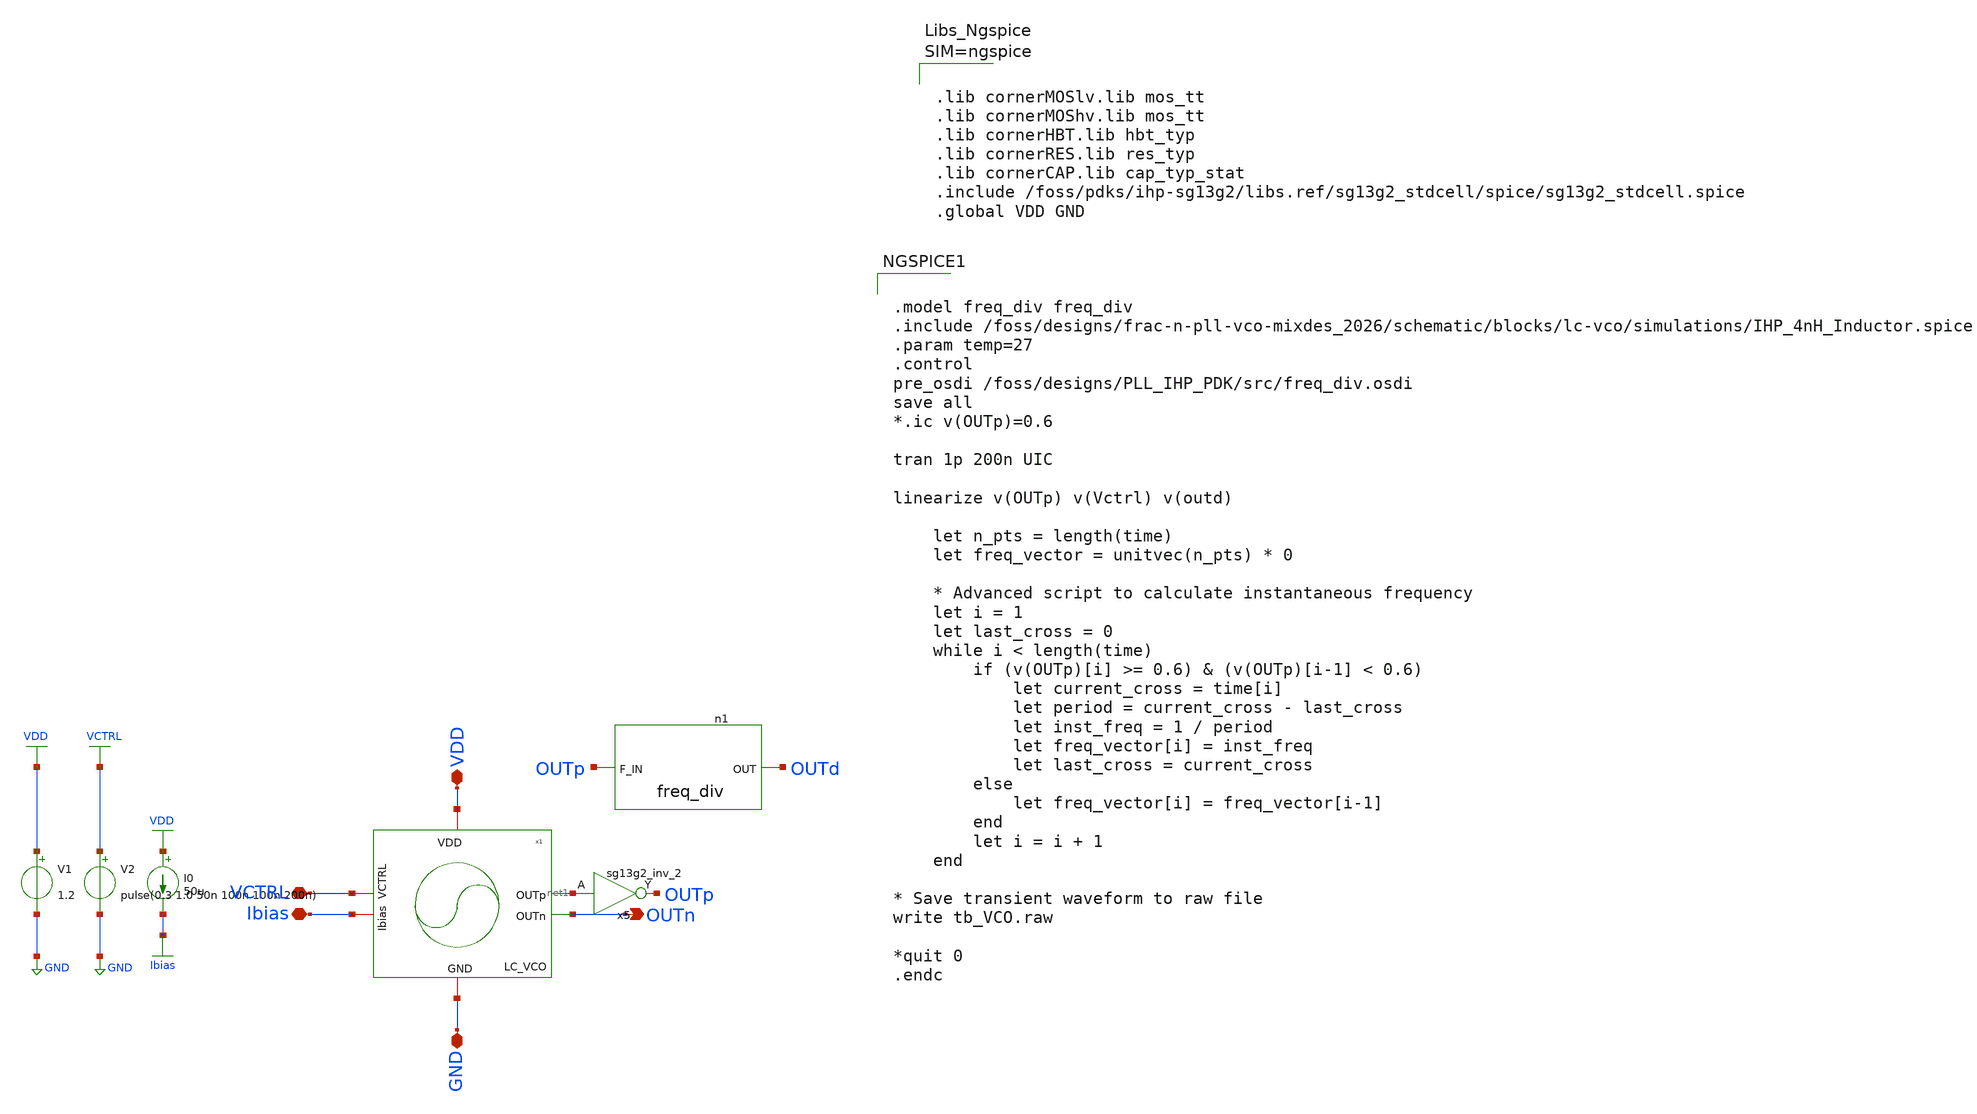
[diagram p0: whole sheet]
** sch_path: schematic/blocks/PLL_IHP/tb/tb_VCO.sch
* IHP-GmbH/IHP-Open-PDK/ihp-sg13g2/libs.tech/xschem/sg13g2_stdcells/sg13g2_inv_2.sch:
* Copyright 2023 IHP PDK Authors
* Licensed under the Apache License, Version 2.0 (the "License");
**.subckt tb_VCO OUTn VDD VCTRL GND Ibias
*.opin OUTn
*.iopin VDD
*.iopin VCTRL
*.iopin GND
*.iopin Ibias
V1 VDD GND 1.2
V2 VCTRL GND pulse(0.3 1.0 50n 100n 100n 200n)
I0 VDD Ibias 50u
x2 VDD net1 OUTn Ibias VCTRL GND LC_VCO
n1 OUTd OUTp freq_div
x5 OUTp net1 VDD GND sg13g2_inv_2
**** begin user architecture code


.model freq_div freq_div
.include /foss/designs/frac-n-pll-vco-mixdes_2026/schematic/blocks/lc-vco/simulations/IHP_4nH_Inductor.spice
.param temp=27
.control
pre_osdi /foss/designs/PLL_IHP_PDK/src/freq_div.osdi
save all
*.ic v(OUTp)=0.6

tran 1p 200n UIC

linearize v(OUTp) v(Vctrl) v(outd)

    let n_pts = length(time)
    let freq_vector = unitvec(n_pts) * 0

    * Advanced script to calculate instantaneous frequency
    let i = 1
    let last_cross = 0
    while i < length(time)
        if (v(OUTp)[i] >= 0.6) & (v(OUTp)[i-1] < 0.6)
            let current_cross = time[i]
            let period = current_cross - last_cross
            let inst_freq = 1 / period
            let freq_vector[i] = inst_freq
            let last_cross = current_cross
        else
            let freq_vector[i] = freq_vector[i-1]
        end
        let i = i + 1
    end

* Save transient waveform to raw file
write tb_VCO.raw

*quit 0
.endc





.lib cornerMOSlv.lib mos_tt
.lib cornerMOShv.lib mos_tt
.lib cornerHBT.lib hbt_typ
.lib cornerRES.lib res_typ
.lib cornerCAP.lib cap_typ_stat
.include /foss/pdks/ihp-sg13g2/libs.ref/sg13g2_stdcell/spice/sg13g2_stdcell.spice
.global VDD GND




**** end user architecture code
**.ends

* expanding   symbol:  /foss/designs/frac-n-pll-vco-mixdes_2026/schematic/blocks/lc-vco/LC_VCO.sym #
*+ of pins=6
** sym_path: /foss/designs/frac-n-pll-vco-mixdes_2026/schematic/blocks/lc-vco/LC_VCO.sym
** sch_path: /foss/designs/frac-n-pll-vco-mixdes_2026/schematic/blocks/lc-vco/LC_VCO.sch
.subckt LC_VCO VDD OUTp OUTn Ibias VCTRL GND
*.iopin VDD
*.opin OUTp
*.opin OUTn
*.iopin GND
*.iopin VCTRL
*.iopin Ibias
XM6 net1 Ibias GND GND sg13_lv_nmos w=1u l=0.15u ng=1 m=60 mm_ok=1
XM5 Ibias Ibias GND GND sg13_lv_nmos w=1u l=0.15u ng=1 m=1 mm_ok=1
XM4 OUTp OUTn VDD VDD sg13_lv_pmos w=8.5u l=0.5u ng=1 m=13 mm_ok=1
X5M3 OUTn OUTp VDD VDD sg13_lv_pmos w=8.5u l=0.5u ng=1 m=13 mm_ok=1
XM2 OUTp OUTn net1 GND sg13_lv_nmos w=2u l=0.5u ng=1 m=12 mm_ok=1
XM1 OUTn OUTp net1 GND sg13_lv_nmos w=2u l=0.5u ng=1 m=12 mm_ok=1
XC3 OUTp OUTn cap_cmim w=4.0e-6 l=4.0e-6 m=13.6 mm_ok=1
XMv2 OUTp VCTRL OUTp VDD sg13_lv_pmos w=4u l=4u ng=1 m=22 mm_ok=1
XMv1 OUTn VCTRL OUTn VDD sg13_lv_pmos w=4u l=4u ng=1 m=22 mm_ok=1
XR1 OUTp OUTn sub! rhigh w=1e-6 l=1e-6 m=1.23 b=0 mm_ok=1
x1 OUTn OUTp ihp_4nh_inductor
.ends


* expanding   symbol:  sg13g2_stdcells/sg13g2_inv_2.sym # of pins=2
** sym_path: sg13g2_stdcells/sg13g2_inv_2.sym
** sch_path: sg13g2_stdcells/sg13g2_inv_2.sch
.subckt sg13g2_inv_2 Y A VDD VSS
*.opin Y
*.ipin A
*.iopin VDD
*.iopin VSS
XM1 Y A VSS VSS sg13_lv_nmos w=1.48u l=130.00n ng=2 m=1 mm_ok=1
XM2 Y A VDD VDD sg13_lv_pmos w=2.24u l=130.00n ng=2 m=1 mm_ok=1
.ends

.GLOBAL GND
.GLOBAL VDD
.GLOBAL VCTRL
.GLOBAL Ibias
.end
